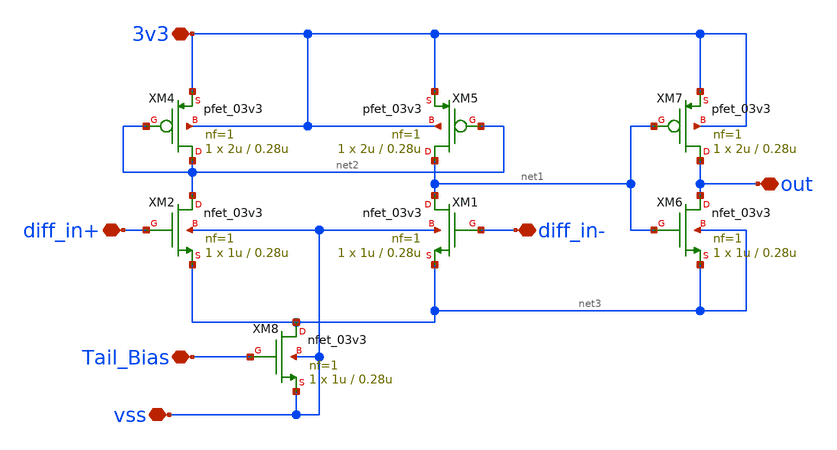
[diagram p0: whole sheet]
** sch_path: analog/Differential_Buffer/Differential_Buffer.sch
**.subckt Differential_Buffer 3v3 vss diff_in+ diff_in- out Tail_Bias
*.iopin 3v3
*.iopin vss
*.iopin diff_in+
*.iopin diff_in-
*.iopin out
*.iopin Tail_Bias
XM1 net1 diff_in- net3 vss nfet_03v3 L=0.28u W=1u nf=1 ad='int((nf+1)/2) * W/nf * 0.18u' as='int((nf+2)/2) * W/nf * 0.18u'
+ pd='2*int((nf+1)/2) * (W/nf + 0.18u)' ps='2*int((nf+2)/2) * (W/nf + 0.18u)' nrd='0.18u / W' nrs='0.18u / W'
+ sa=0 sb=0 sd=0 m=1
XM2 net2 diff_in+ net3 vss nfet_03v3 L=0.28u W=1u nf=1 ad='int((nf+1)/2) * W/nf * 0.18u' as='int((nf+2)/2) * W/nf * 0.18u'
+ pd='2*int((nf+1)/2) * (W/nf + 0.18u)' ps='2*int((nf+2)/2) * (W/nf + 0.18u)' nrd='0.18u / W' nrs='0.18u / W'
+ sa=0 sb=0 sd=0 m=1
XM4 net2 net2 3v3 3v3 pfet_03v3 L=0.28u W=2u nf=1 ad='int((nf+1)/2) * W/nf * 0.18u' as='int((nf+2)/2) * W/nf * 0.18u'
+ pd='2*int((nf+1)/2) * (W/nf + 0.18u)' ps='2*int((nf+2)/2) * (W/nf + 0.18u)' nrd='0.18u / W' nrs='0.18u / W'
+ sa=0 sb=0 sd=0 m=1
XM5 net1 net2 3v3 3v3 pfet_03v3 L=0.28u W=2u nf=1 ad='int((nf+1)/2) * W/nf * 0.18u' as='int((nf+2)/2) * W/nf * 0.18u'
+ pd='2*int((nf+1)/2) * (W/nf + 0.18u)' ps='2*int((nf+2)/2) * (W/nf + 0.18u)' nrd='0.18u / W' nrs='0.18u / W'
+ sa=0 sb=0 sd=0 m=1
XM6 out net1 net3 net3 nfet_03v3 L=0.28u W=1u nf=1 ad='int((nf+1)/2) * W/nf * 0.18u' as='int((nf+2)/2) * W/nf * 0.18u'
+ pd='2*int((nf+1)/2) * (W/nf + 0.18u)' ps='2*int((nf+2)/2) * (W/nf + 0.18u)' nrd='0.18u / W' nrs='0.18u / W'
+ sa=0 sb=0 sd=0 m=1
XM7 out net1 3v3 3v3 pfet_03v3 L=0.28u W=2u nf=1 ad='int((nf+1)/2) * W/nf * 0.18u' as='int((nf+2)/2) * W/nf * 0.18u'
+ pd='2*int((nf+1)/2) * (W/nf + 0.18u)' ps='2*int((nf+2)/2) * (W/nf + 0.18u)' nrd='0.18u / W' nrs='0.18u / W'
+ sa=0 sb=0 sd=0 m=1
XM8 net3 Tail_Bias vss vss nfet_03v3 L=0.28u W=1u nf=1 ad='int((nf+1)/2) * W/nf * 0.18u' as='int((nf+2)/2) * W/nf * 0.18u'
+ pd='2*int((nf+1)/2) * (W/nf + 0.18u)' ps='2*int((nf+2)/2) * (W/nf + 0.18u)' nrd='0.18u / W' nrs='0.18u / W'
+ sa=0 sb=0 sd=0 m=1
**.ends
.end
